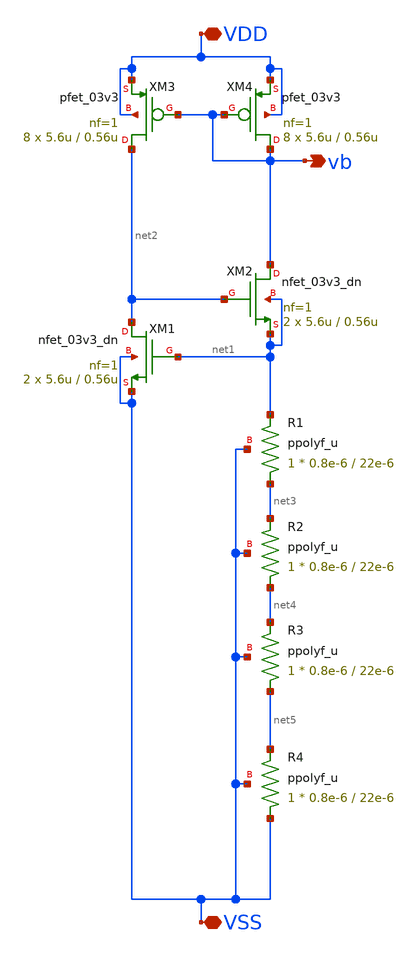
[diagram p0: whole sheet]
** sch_path: CS/cs_vthref_3ho.sch
**.subckt cs_vthref_3ho VSS VDD vb
*.iopin VSS
*.iopin VDD
*.opin vb
XM4 vb vb VDD VDD pfet_03v3 L=0.56u W=5.6u nf=1 ad='int((nf+1)/2) * W/nf * 0.18u' as='int((nf+2)/2) * W/nf * 0.18u'
+ pd='2*int((nf+1)/2) * (W/nf + 0.18u)' ps='2*int((nf+2)/2) * (W/nf + 0.18u)' nrd='0.18u / W' nrs='0.18u / W'
+ sa=0 sb=0 sd=0 m=8
XM3 net2 vb VDD VDD pfet_03v3 L=0.56u W=5.6u nf=1 ad='int((nf+1)/2) * W/nf * 0.18u' as='int((nf+2)/2) * W/nf * 0.18u'
+ pd='2*int((nf+1)/2) * (W/nf + 0.18u)' ps='2*int((nf+2)/2) * (W/nf + 0.18u)' nrd='0.18u / W' nrs='0.18u / W'
+ sa=0 sb=0 sd=0 m=8
XM2 vb net2 net1 net1 nfet_03v3_dn L=0.56u W=5.6u nf=1 ad='int((nf+1)/2) * W/nf * 0.18u' as='int((nf+2)/2) * W/nf * 0.18u'
+ pd='2*int((nf+1)/2) * (W/nf + 0.18u)' ps='2*int((nf+2)/2) * (W/nf + 0.18u)' nrd='0.18u / W' nrs='0.18u / W'
+ sa=0 sb=0 sd=0 m=2
XM1 net2 net1 VSS VSS nfet_03v3_dn L=0.56u W=5.6u nf=1 ad='int((nf+1)/2) * W/nf * 0.18u' as='int((nf+2)/2) * W/nf * 0.18u'
+ pd='2*int((nf+1)/2) * (W/nf + 0.18u)' ps='2*int((nf+2)/2) * (W/nf + 0.18u)' nrd='0.18u / W' nrs='0.18u / W'
+ sa=0 sb=0 sd=0 m=2
XR3 net5 net4 VSS ppolyf_u r_width=0.8e-6 r_length=22e-6 m=1
XR4 VSS net5 VSS ppolyf_u r_width=0.8e-6 r_length=22e-6 m=1
XR1 net3 net1 VSS ppolyf_u r_width=0.8e-6 r_length=22e-6 m=1
XR2 net4 net3 VSS ppolyf_u r_width=0.8e-6 r_length=22e-6 m=1
**.ends
.end
